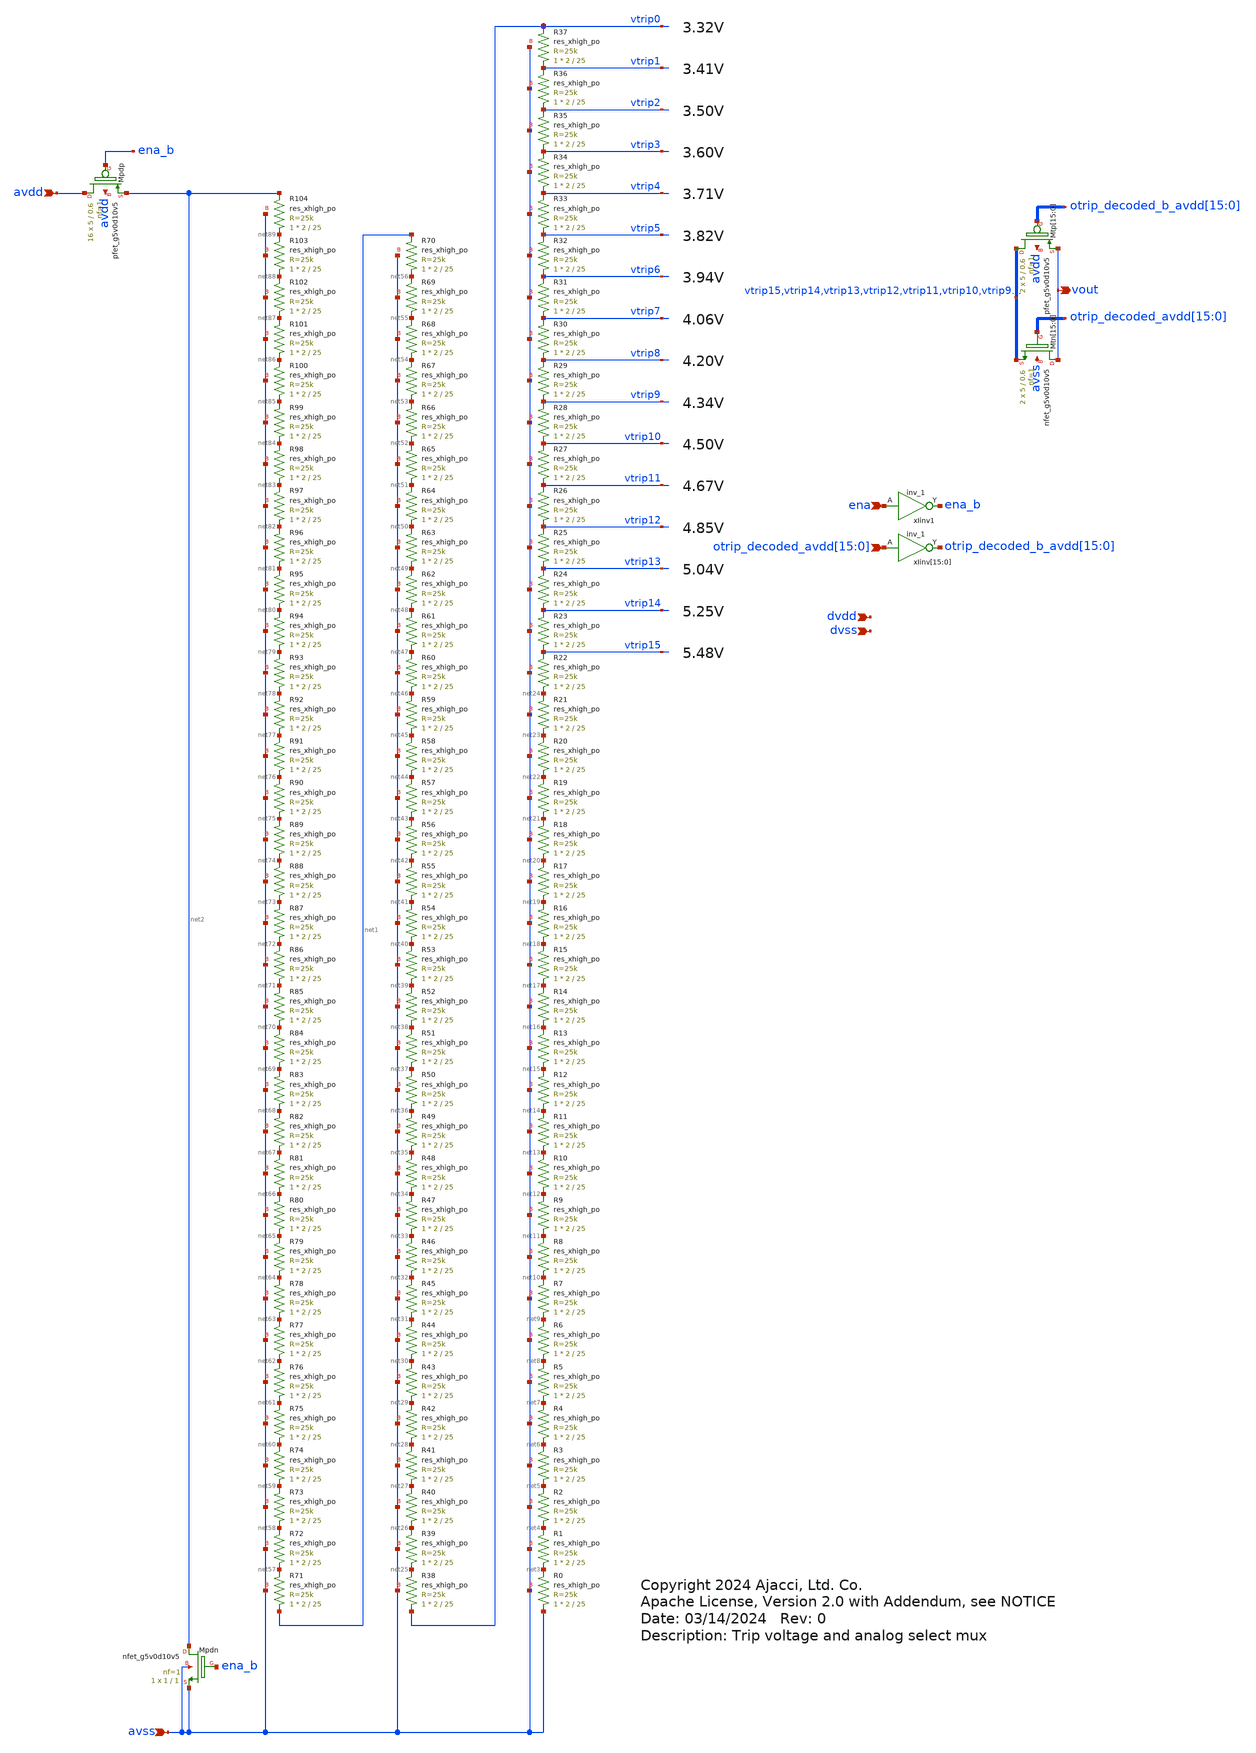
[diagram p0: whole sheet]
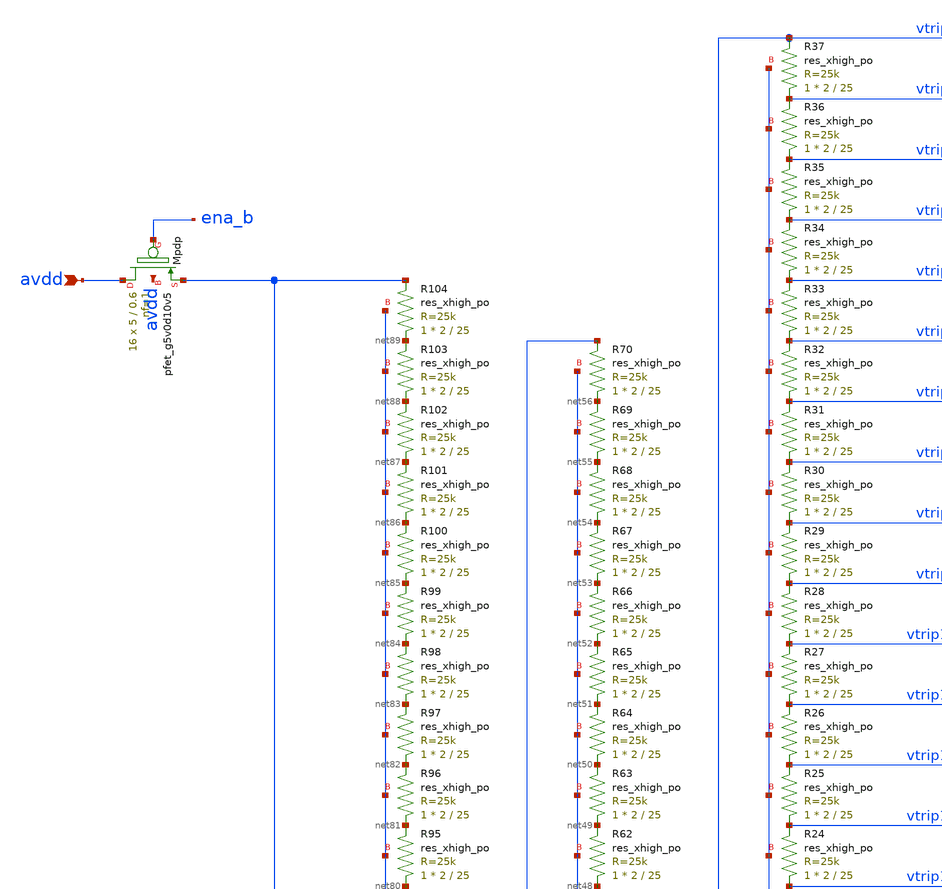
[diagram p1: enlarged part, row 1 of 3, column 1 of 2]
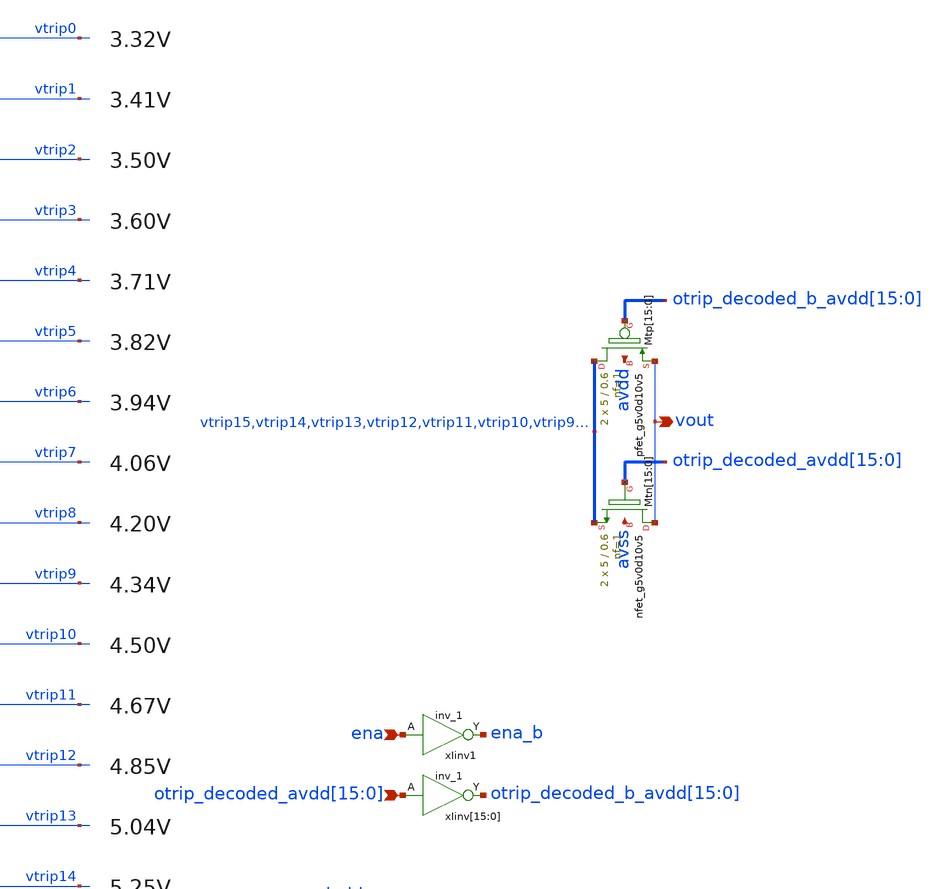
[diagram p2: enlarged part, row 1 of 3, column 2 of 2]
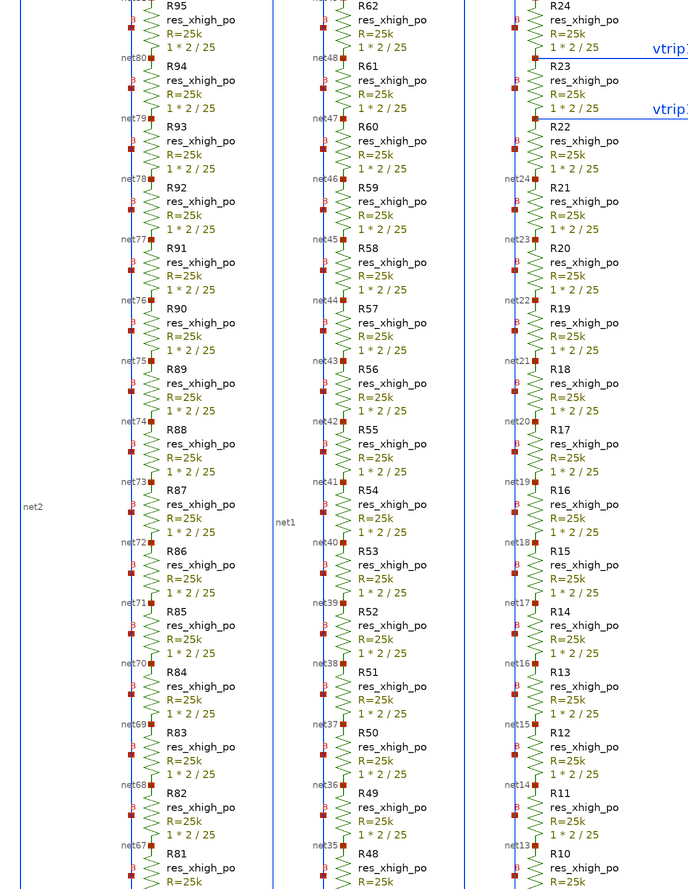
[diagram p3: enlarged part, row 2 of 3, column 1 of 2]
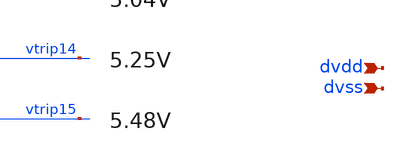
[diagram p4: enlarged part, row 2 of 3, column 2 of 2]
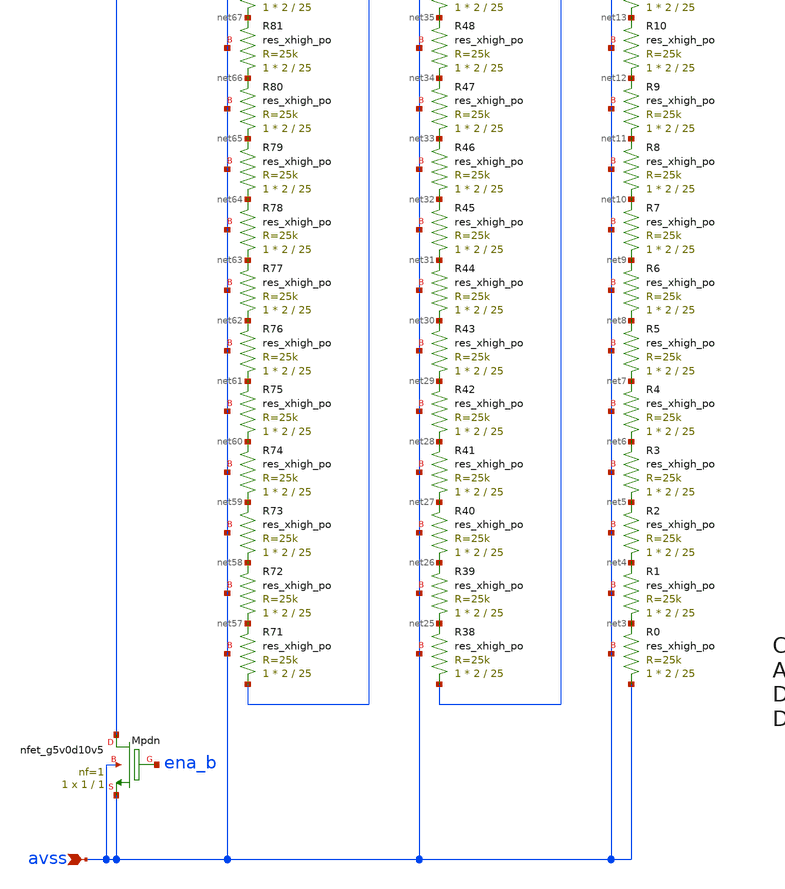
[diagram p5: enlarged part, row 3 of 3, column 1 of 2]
** sch_path: xschem/rstring_mux.sch
* Copyright 2024 Ajacci, Ltd. Co.
* Apache License, Version 2.0 with Addendum, see NOTICE
**.subckt rstring_mux vout
*+ otrip_decoded_avdd[15],otrip_decoded_avdd[14],otrip_decoded_avdd[13],otrip_decoded_avdd[12],otrip_decoded_avdd[11],otrip_decoded_avdd[10],otrip_decoded_avdd[9],otrip_decoded_avdd[8],otrip_decoded_avdd[7],otrip_decoded_avdd[6],otrip_decoded_avdd[5],otrip_decoded_avdd[4],otrip_decoded_avdd[3],otrip_decoded_avdd[2],otrip_decoded_avdd[1],otrip_decoded_avdd[0] dvss dvdd avdd avss ena
*.opin vout
*.ipin
*+ otrip_decoded_avdd[15],otrip_decoded_avdd[14],otrip_decoded_avdd[13],otrip_decoded_avdd[12],otrip_decoded_avdd[11],otrip_decoded_avdd[10],otrip_decoded_avdd[9],otrip_decoded_avdd[8],otrip_decoded_avdd[7],otrip_decoded_avdd[6],otrip_decoded_avdd[5],otrip_decoded_avdd[4],otrip_decoded_avdd[3],otrip_decoded_avdd[2],otrip_decoded_avdd[1],otrip_decoded_avdd[0]
*.ipin dvss
*.ipin dvdd
*.ipin avdd
*.ipin avss
*.ipin ena
XR1 net3 net4 avss sky130_fd_pr__res_xhigh_po W=2 L=25 mult=1 m=1
XR2 net4 net5 avss sky130_fd_pr__res_xhigh_po W=2 L=25 mult=1 m=1
XR3 net5 net6 avss sky130_fd_pr__res_xhigh_po W=2 L=25 mult=1 m=1
XR4 net6 net7 avss sky130_fd_pr__res_xhigh_po W=2 L=25 mult=1 m=1
XR5 net7 net8 avss sky130_fd_pr__res_xhigh_po W=2 L=25 mult=1 m=1
XR6 net8 net9 avss sky130_fd_pr__res_xhigh_po W=2 L=25 mult=1 m=1
XR7 net9 net10 avss sky130_fd_pr__res_xhigh_po W=2 L=25 mult=1 m=1
XR8 net10 net11 avss sky130_fd_pr__res_xhigh_po W=2 L=25 mult=1 m=1
XR9 net11 net12 avss sky130_fd_pr__res_xhigh_po W=2 L=25 mult=1 m=1
XR10 net12 net13 avss sky130_fd_pr__res_xhigh_po W=2 L=25 mult=1 m=1
XR11 net13 net14 avss sky130_fd_pr__res_xhigh_po W=2 L=25 mult=1 m=1
XR12 net14 net15 avss sky130_fd_pr__res_xhigh_po W=2 L=25 mult=1 m=1
XR13 net15 net16 avss sky130_fd_pr__res_xhigh_po W=2 L=25 mult=1 m=1
XR14 net16 net17 avss sky130_fd_pr__res_xhigh_po W=2 L=25 mult=1 m=1
XR15 net17 net18 avss sky130_fd_pr__res_xhigh_po W=2 L=25 mult=1 m=1
XR16 net18 net19 avss sky130_fd_pr__res_xhigh_po W=2 L=25 mult=1 m=1
XR17 net19 net20 avss sky130_fd_pr__res_xhigh_po W=2 L=25 mult=1 m=1
XR18 net20 net21 avss sky130_fd_pr__res_xhigh_po W=2 L=25 mult=1 m=1
XR19 net21 net22 avss sky130_fd_pr__res_xhigh_po W=2 L=25 mult=1 m=1
XR20 net22 net23 avss sky130_fd_pr__res_xhigh_po W=2 L=25 mult=1 m=1
XR21 net23 net24 avss sky130_fd_pr__res_xhigh_po W=2 L=25 mult=1 m=1
XR22 net24 vtrip15 avss sky130_fd_pr__res_xhigh_po W=2 L=25 mult=1 m=1
XR23 vtrip15 vtrip14 avss sky130_fd_pr__res_xhigh_po W=2 L=25 mult=1 m=1
XR24 vtrip14 vtrip13 avss sky130_fd_pr__res_xhigh_po W=2 L=25 mult=1 m=1
XR25 vtrip13 vtrip12 avss sky130_fd_pr__res_xhigh_po W=2 L=25 mult=1 m=1
XR26 vtrip12 vtrip11 avss sky130_fd_pr__res_xhigh_po W=2 L=25 mult=1 m=1
XR27 vtrip11 vtrip10 avss sky130_fd_pr__res_xhigh_po W=2 L=25 mult=1 m=1
XR28 vtrip10 vtrip9 avss sky130_fd_pr__res_xhigh_po W=2 L=25 mult=1 m=1
XR29 vtrip9 vtrip8 avss sky130_fd_pr__res_xhigh_po W=2 L=25 mult=1 m=1
XR30 vtrip8 vtrip7 avss sky130_fd_pr__res_xhigh_po W=2 L=25 mult=1 m=1
XR31 vtrip7 vtrip6 avss sky130_fd_pr__res_xhigh_po W=2 L=25 mult=1 m=1
XR32 vtrip6 vtrip5 avss sky130_fd_pr__res_xhigh_po W=2 L=25 mult=1 m=1
XR33 vtrip5 vtrip4 avss sky130_fd_pr__res_xhigh_po W=2 L=25 mult=1 m=1
XR34 vtrip4 vtrip3 avss sky130_fd_pr__res_xhigh_po W=2 L=25 mult=1 m=1
XR35 vtrip3 vtrip2 avss sky130_fd_pr__res_xhigh_po W=2 L=25 mult=1 m=1
XR36 vtrip2 vtrip1 avss sky130_fd_pr__res_xhigh_po W=2 L=25 mult=1 m=1
XR37 vtrip1 vtrip0 avss sky130_fd_pr__res_xhigh_po W=2 L=25 mult=1 m=1
XR38 vtrip0 net25 avss sky130_fd_pr__res_xhigh_po W=2 L=25 mult=1 m=1
XR39 net25 net26 avss sky130_fd_pr__res_xhigh_po W=2 L=25 mult=1 m=1
XR40 net26 net27 avss sky130_fd_pr__res_xhigh_po W=2 L=25 mult=1 m=1
XR41 net27 net28 avss sky130_fd_pr__res_xhigh_po W=2 L=25 mult=1 m=1
XR42 net28 net29 avss sky130_fd_pr__res_xhigh_po W=2 L=25 mult=1 m=1
XR43 net29 net30 avss sky130_fd_pr__res_xhigh_po W=2 L=25 mult=1 m=1
XR44 net30 net31 avss sky130_fd_pr__res_xhigh_po W=2 L=25 mult=1 m=1
XR45 net31 net32 avss sky130_fd_pr__res_xhigh_po W=2 L=25 mult=1 m=1
XR46 net32 net33 avss sky130_fd_pr__res_xhigh_po W=2 L=25 mult=1 m=1
XR47 net33 net34 avss sky130_fd_pr__res_xhigh_po W=2 L=25 mult=1 m=1
XR48 net34 net35 avss sky130_fd_pr__res_xhigh_po W=2 L=25 mult=1 m=1
XR49 net35 net36 avss sky130_fd_pr__res_xhigh_po W=2 L=25 mult=1 m=1
XR50 net36 net37 avss sky130_fd_pr__res_xhigh_po W=2 L=25 mult=1 m=1
XR51 net37 net38 avss sky130_fd_pr__res_xhigh_po W=2 L=25 mult=1 m=1
XR52 net38 net39 avss sky130_fd_pr__res_xhigh_po W=2 L=25 mult=1 m=1
XR53 net39 net40 avss sky130_fd_pr__res_xhigh_po W=2 L=25 mult=1 m=1
XR54 net40 net41 avss sky130_fd_pr__res_xhigh_po W=2 L=25 mult=1 m=1
XR55 net41 net42 avss sky130_fd_pr__res_xhigh_po W=2 L=25 mult=1 m=1
XR56 net42 net43 avss sky130_fd_pr__res_xhigh_po W=2 L=25 mult=1 m=1
XR57 net43 net44 avss sky130_fd_pr__res_xhigh_po W=2 L=25 mult=1 m=1
XR58 net44 net45 avss sky130_fd_pr__res_xhigh_po W=2 L=25 mult=1 m=1
XR59 net45 net46 avss sky130_fd_pr__res_xhigh_po W=2 L=25 mult=1 m=1
XR60 net46 net47 avss sky130_fd_pr__res_xhigh_po W=2 L=25 mult=1 m=1
XR61 net47 net48 avss sky130_fd_pr__res_xhigh_po W=2 L=25 mult=1 m=1
XR62 net48 net49 avss sky130_fd_pr__res_xhigh_po W=2 L=25 mult=1 m=1
XR63 net49 net50 avss sky130_fd_pr__res_xhigh_po W=2 L=25 mult=1 m=1
XR64 net50 net51 avss sky130_fd_pr__res_xhigh_po W=2 L=25 mult=1 m=1
XR65 net51 net52 avss sky130_fd_pr__res_xhigh_po W=2 L=25 mult=1 m=1
XR66 net52 net53 avss sky130_fd_pr__res_xhigh_po W=2 L=25 mult=1 m=1
XR67 net53 net54 avss sky130_fd_pr__res_xhigh_po W=2 L=25 mult=1 m=1
XR68 net54 net55 avss sky130_fd_pr__res_xhigh_po W=2 L=25 mult=1 m=1
XR69 net55 net56 avss sky130_fd_pr__res_xhigh_po W=2 L=25 mult=1 m=1
XMtp[15] vtrip15 otrip_decoded_b_avdd[15] vout avdd sky130_fd_pr__pfet_g5v0d10v5 L=0.6 W=5 nf=1 ad='int((nf+1)/2) * W/nf * 0.29'
+ as='int((nf+2)/2) * W/nf * 0.29' pd='2*int((nf+1)/2) * (W/nf + 0.29)' ps='2*int((nf+2)/2) * (W/nf + 0.29)'
+ nrd='0.29 / W' nrs='0.29 / W' sa=0 sb=0 sd=0 mult=2 m=2
XMtp[14] vtrip14 otrip_decoded_b_avdd[14] vout avdd sky130_fd_pr__pfet_g5v0d10v5 L=0.6 W=5 nf=1 ad='int((nf+1)/2) * W/nf * 0.29'
+ as='int((nf+2)/2) * W/nf * 0.29' pd='2*int((nf+1)/2) * (W/nf + 0.29)' ps='2*int((nf+2)/2) * (W/nf + 0.29)'
+ nrd='0.29 / W' nrs='0.29 / W' sa=0 sb=0 sd=0 mult=2 m=2
XMtp[13] vtrip13 otrip_decoded_b_avdd[13] vout avdd sky130_fd_pr__pfet_g5v0d10v5 L=0.6 W=5 nf=1 ad='int((nf+1)/2) * W/nf * 0.29'
+ as='int((nf+2)/2) * W/nf * 0.29' pd='2*int((nf+1)/2) * (W/nf + 0.29)' ps='2*int((nf+2)/2) * (W/nf + 0.29)'
+ nrd='0.29 / W' nrs='0.29 / W' sa=0 sb=0 sd=0 mult=2 m=2
XMtp[12] vtrip12 otrip_decoded_b_avdd[12] vout avdd sky130_fd_pr__pfet_g5v0d10v5 L=0.6 W=5 nf=1 ad='int((nf+1)/2) * W/nf * 0.29'
+ as='int((nf+2)/2) * W/nf * 0.29' pd='2*int((nf+1)/2) * (W/nf + 0.29)' ps='2*int((nf+2)/2) * (W/nf + 0.29)'
+ nrd='0.29 / W' nrs='0.29 / W' sa=0 sb=0 sd=0 mult=2 m=2
XMtp[11] vtrip11 otrip_decoded_b_avdd[11] vout avdd sky130_fd_pr__pfet_g5v0d10v5 L=0.6 W=5 nf=1 ad='int((nf+1)/2) * W/nf * 0.29'
+ as='int((nf+2)/2) * W/nf * 0.29' pd='2*int((nf+1)/2) * (W/nf + 0.29)' ps='2*int((nf+2)/2) * (W/nf + 0.29)'
+ nrd='0.29 / W' nrs='0.29 / W' sa=0 sb=0 sd=0 mult=2 m=2
XMtp[10] vtrip10 otrip_decoded_b_avdd[10] vout avdd sky130_fd_pr__pfet_g5v0d10v5 L=0.6 W=5 nf=1 ad='int((nf+1)/2) * W/nf * 0.29'
+ as='int((nf+2)/2) * W/nf * 0.29' pd='2*int((nf+1)/2) * (W/nf + 0.29)' ps='2*int((nf+2)/2) * (W/nf + 0.29)'
+ nrd='0.29 / W' nrs='0.29 / W' sa=0 sb=0 sd=0 mult=2 m=2
XMtp[9] vtrip9 otrip_decoded_b_avdd[9] vout avdd sky130_fd_pr__pfet_g5v0d10v5 L=0.6 W=5 nf=1 ad='int((nf+1)/2) * W/nf * 0.29'
+ as='int((nf+2)/2) * W/nf * 0.29' pd='2*int((nf+1)/2) * (W/nf + 0.29)' ps='2*int((nf+2)/2) * (W/nf + 0.29)'
+ nrd='0.29 / W' nrs='0.29 / W' sa=0 sb=0 sd=0 mult=2 m=2
XMtp[8] vtrip8 otrip_decoded_b_avdd[8] vout avdd sky130_fd_pr__pfet_g5v0d10v5 L=0.6 W=5 nf=1 ad='int((nf+1)/2) * W/nf * 0.29'
+ as='int((nf+2)/2) * W/nf * 0.29' pd='2*int((nf+1)/2) * (W/nf + 0.29)' ps='2*int((nf+2)/2) * (W/nf + 0.29)'
+ nrd='0.29 / W' nrs='0.29 / W' sa=0 sb=0 sd=0 mult=2 m=2
XMtp[7] vtrip7 otrip_decoded_b_avdd[7] vout avdd sky130_fd_pr__pfet_g5v0d10v5 L=0.6 W=5 nf=1 ad='int((nf+1)/2) * W/nf * 0.29'
+ as='int((nf+2)/2) * W/nf * 0.29' pd='2*int((nf+1)/2) * (W/nf + 0.29)' ps='2*int((nf+2)/2) * (W/nf + 0.29)'
+ nrd='0.29 / W' nrs='0.29 / W' sa=0 sb=0 sd=0 mult=2 m=2
XMtp[6] vtrip6 otrip_decoded_b_avdd[6] vout avdd sky130_fd_pr__pfet_g5v0d10v5 L=0.6 W=5 nf=1 ad='int((nf+1)/2) * W/nf * 0.29'
+ as='int((nf+2)/2) * W/nf * 0.29' pd='2*int((nf+1)/2) * (W/nf + 0.29)' ps='2*int((nf+2)/2) * (W/nf + 0.29)'
+ nrd='0.29 / W' nrs='0.29 / W' sa=0 sb=0 sd=0 mult=2 m=2
XMtp[5] vtrip5 otrip_decoded_b_avdd[5] vout avdd sky130_fd_pr__pfet_g5v0d10v5 L=0.6 W=5 nf=1 ad='int((nf+1)/2) * W/nf * 0.29'
+ as='int((nf+2)/2) * W/nf * 0.29' pd='2*int((nf+1)/2) * (W/nf + 0.29)' ps='2*int((nf+2)/2) * (W/nf + 0.29)'
+ nrd='0.29 / W' nrs='0.29 / W' sa=0 sb=0 sd=0 mult=2 m=2
XMtp[4] vtrip4 otrip_decoded_b_avdd[4] vout avdd sky130_fd_pr__pfet_g5v0d10v5 L=0.6 W=5 nf=1 ad='int((nf+1)/2) * W/nf * 0.29'
+ as='int((nf+2)/2) * W/nf * 0.29' pd='2*int((nf+1)/2) * (W/nf + 0.29)' ps='2*int((nf+2)/2) * (W/nf + 0.29)'
+ nrd='0.29 / W' nrs='0.29 / W' sa=0 sb=0 sd=0 mult=2 m=2
XMtp[3] vtrip3 otrip_decoded_b_avdd[3] vout avdd sky130_fd_pr__pfet_g5v0d10v5 L=0.6 W=5 nf=1 ad='int((nf+1)/2) * W/nf * 0.29'
+ as='int((nf+2)/2) * W/nf * 0.29' pd='2*int((nf+1)/2) * (W/nf + 0.29)' ps='2*int((nf+2)/2) * (W/nf + 0.29)'
+ nrd='0.29 / W' nrs='0.29 / W' sa=0 sb=0 sd=0 mult=2 m=2
XMtp[2] vtrip2 otrip_decoded_b_avdd[2] vout avdd sky130_fd_pr__pfet_g5v0d10v5 L=0.6 W=5 nf=1 ad='int((nf+1)/2) * W/nf * 0.29'
+ as='int((nf+2)/2) * W/nf * 0.29' pd='2*int((nf+1)/2) * (W/nf + 0.29)' ps='2*int((nf+2)/2) * (W/nf + 0.29)'
+ nrd='0.29 / W' nrs='0.29 / W' sa=0 sb=0 sd=0 mult=2 m=2
XMtp[1] vtrip1 otrip_decoded_b_avdd[1] vout avdd sky130_fd_pr__pfet_g5v0d10v5 L=0.6 W=5 nf=1 ad='int((nf+1)/2) * W/nf * 0.29'
+ as='int((nf+2)/2) * W/nf * 0.29' pd='2*int((nf+1)/2) * (W/nf + 0.29)' ps='2*int((nf+2)/2) * (W/nf + 0.29)'
+ nrd='0.29 / W' nrs='0.29 / W' sa=0 sb=0 sd=0 mult=2 m=2
XMtp[0] vtrip0 otrip_decoded_b_avdd[0] vout avdd sky130_fd_pr__pfet_g5v0d10v5 L=0.6 W=5 nf=1 ad='int((nf+1)/2) * W/nf * 0.29'
+ as='int((nf+2)/2) * W/nf * 0.29' pd='2*int((nf+1)/2) * (W/nf + 0.29)' ps='2*int((nf+2)/2) * (W/nf + 0.29)'
+ nrd='0.29 / W' nrs='0.29 / W' sa=0 sb=0 sd=0 mult=2 m=2
XMtn[15] vout otrip_decoded_avdd[15] vtrip15 avss sky130_fd_pr__nfet_g5v0d10v5 L=0.6 W=5 nf=1 ad='int((nf+1)/2) * W/nf * 0.29'
+ as='int((nf+2)/2) * W/nf * 0.29' pd='2*int((nf+1)/2) * (W/nf + 0.29)' ps='2*int((nf+2)/2) * (W/nf + 0.29)'
+ nrd='0.29 / W' nrs='0.29 / W' sa=0 sb=0 sd=0 mult=2 m=2
XMtn[14] vout otrip_decoded_avdd[14] vtrip14 avss sky130_fd_pr__nfet_g5v0d10v5 L=0.6 W=5 nf=1 ad='int((nf+1)/2) * W/nf * 0.29'
+ as='int((nf+2)/2) * W/nf * 0.29' pd='2*int((nf+1)/2) * (W/nf + 0.29)' ps='2*int((nf+2)/2) * (W/nf + 0.29)'
+ nrd='0.29 / W' nrs='0.29 / W' sa=0 sb=0 sd=0 mult=2 m=2
XMtn[13] vout otrip_decoded_avdd[13] vtrip13 avss sky130_fd_pr__nfet_g5v0d10v5 L=0.6 W=5 nf=1 ad='int((nf+1)/2) * W/nf * 0.29'
+ as='int((nf+2)/2) * W/nf * 0.29' pd='2*int((nf+1)/2) * (W/nf + 0.29)' ps='2*int((nf+2)/2) * (W/nf + 0.29)'
+ nrd='0.29 / W' nrs='0.29 / W' sa=0 sb=0 sd=0 mult=2 m=2
XMtn[12] vout otrip_decoded_avdd[12] vtrip12 avss sky130_fd_pr__nfet_g5v0d10v5 L=0.6 W=5 nf=1 ad='int((nf+1)/2) * W/nf * 0.29'
+ as='int((nf+2)/2) * W/nf * 0.29' pd='2*int((nf+1)/2) * (W/nf + 0.29)' ps='2*int((nf+2)/2) * (W/nf + 0.29)'
+ nrd='0.29 / W' nrs='0.29 / W' sa=0 sb=0 sd=0 mult=2 m=2
XMtn[11] vout otrip_decoded_avdd[11] vtrip11 avss sky130_fd_pr__nfet_g5v0d10v5 L=0.6 W=5 nf=1 ad='int((nf+1)/2) * W/nf * 0.29'
+ as='int((nf+2)/2) * W/nf * 0.29' pd='2*int((nf+1)/2) * (W/nf + 0.29)' ps='2*int((nf+2)/2) * (W/nf + 0.29)'
+ nrd='0.29 / W' nrs='0.29 / W' sa=0 sb=0 sd=0 mult=2 m=2
XMtn[10] vout otrip_decoded_avdd[10] vtrip10 avss sky130_fd_pr__nfet_g5v0d10v5 L=0.6 W=5 nf=1 ad='int((nf+1)/2) * W/nf * 0.29'
+ as='int((nf+2)/2) * W/nf * 0.29' pd='2*int((nf+1)/2) * (W/nf + 0.29)' ps='2*int((nf+2)/2) * (W/nf + 0.29)'
+ nrd='0.29 / W' nrs='0.29 / W' sa=0 sb=0 sd=0 mult=2 m=2
XMtn[9] vout otrip_decoded_avdd[9] vtrip9 avss sky130_fd_pr__nfet_g5v0d10v5 L=0.6 W=5 nf=1 ad='int((nf+1)/2) * W/nf * 0.29'
+ as='int((nf+2)/2) * W/nf * 0.29' pd='2*int((nf+1)/2) * (W/nf + 0.29)' ps='2*int((nf+2)/2) * (W/nf + 0.29)'
+ nrd='0.29 / W' nrs='0.29 / W' sa=0 sb=0 sd=0 mult=2 m=2
XMtn[8] vout otrip_decoded_avdd[8] vtrip8 avss sky130_fd_pr__nfet_g5v0d10v5 L=0.6 W=5 nf=1 ad='int((nf+1)/2) * W/nf * 0.29'
+ as='int((nf+2)/2) * W/nf * 0.29' pd='2*int((nf+1)/2) * (W/nf + 0.29)' ps='2*int((nf+2)/2) * (W/nf + 0.29)'
+ nrd='0.29 / W' nrs='0.29 / W' sa=0 sb=0 sd=0 mult=2 m=2
XMtn[7] vout otrip_decoded_avdd[7] vtrip7 avss sky130_fd_pr__nfet_g5v0d10v5 L=0.6 W=5 nf=1 ad='int((nf+1)/2) * W/nf * 0.29'
+ as='int((nf+2)/2) * W/nf * 0.29' pd='2*int((nf+1)/2) * (W/nf + 0.29)' ps='2*int((nf+2)/2) * (W/nf + 0.29)'
+ nrd='0.29 / W' nrs='0.29 / W' sa=0 sb=0 sd=0 mult=2 m=2
XMtn[6] vout otrip_decoded_avdd[6] vtrip6 avss sky130_fd_pr__nfet_g5v0d10v5 L=0.6 W=5 nf=1 ad='int((nf+1)/2) * W/nf * 0.29'
+ as='int((nf+2)/2) * W/nf * 0.29' pd='2*int((nf+1)/2) * (W/nf + 0.29)' ps='2*int((nf+2)/2) * (W/nf + 0.29)'
+ nrd='0.29 / W' nrs='0.29 / W' sa=0 sb=0 sd=0 mult=2 m=2
XMtn[5] vout otrip_decoded_avdd[5] vtrip5 avss sky130_fd_pr__nfet_g5v0d10v5 L=0.6 W=5 nf=1 ad='int((nf+1)/2) * W/nf * 0.29'
+ as='int((nf+2)/2) * W/nf * 0.29' pd='2*int((nf+1)/2) * (W/nf + 0.29)' ps='2*int((nf+2)/2) * (W/nf + 0.29)'
+ nrd='0.29 / W' nrs='0.29 / W' sa=0 sb=0 sd=0 mult=2 m=2
XMtn[4] vout otrip_decoded_avdd[4] vtrip4 avss sky130_fd_pr__nfet_g5v0d10v5 L=0.6 W=5 nf=1 ad='int((nf+1)/2) * W/nf * 0.29'
+ as='int((nf+2)/2) * W/nf * 0.29' pd='2*int((nf+1)/2) * (W/nf + 0.29)' ps='2*int((nf+2)/2) * (W/nf + 0.29)'
+ nrd='0.29 / W' nrs='0.29 / W' sa=0 sb=0 sd=0 mult=2 m=2
XMtn[3] vout otrip_decoded_avdd[3] vtrip3 avss sky130_fd_pr__nfet_g5v0d10v5 L=0.6 W=5 nf=1 ad='int((nf+1)/2) * W/nf * 0.29'
+ as='int((nf+2)/2) * W/nf * 0.29' pd='2*int((nf+1)/2) * (W/nf + 0.29)' ps='2*int((nf+2)/2) * (W/nf + 0.29)'
+ nrd='0.29 / W' nrs='0.29 / W' sa=0 sb=0 sd=0 mult=2 m=2
XMtn[2] vout otrip_decoded_avdd[2] vtrip2 avss sky130_fd_pr__nfet_g5v0d10v5 L=0.6 W=5 nf=1 ad='int((nf+1)/2) * W/nf * 0.29'
+ as='int((nf+2)/2) * W/nf * 0.29' pd='2*int((nf+1)/2) * (W/nf + 0.29)' ps='2*int((nf+2)/2) * (W/nf + 0.29)'
+ nrd='0.29 / W' nrs='0.29 / W' sa=0 sb=0 sd=0 mult=2 m=2
XMtn[1] vout otrip_decoded_avdd[1] vtrip1 avss sky130_fd_pr__nfet_g5v0d10v5 L=0.6 W=5 nf=1 ad='int((nf+1)/2) * W/nf * 0.29'
+ as='int((nf+2)/2) * W/nf * 0.29' pd='2*int((nf+1)/2) * (W/nf + 0.29)' ps='2*int((nf+2)/2) * (W/nf + 0.29)'
+ nrd='0.29 / W' nrs='0.29 / W' sa=0 sb=0 sd=0 mult=2 m=2
XMtn[0] vout otrip_decoded_avdd[0] vtrip0 avss sky130_fd_pr__nfet_g5v0d10v5 L=0.6 W=5 nf=1 ad='int((nf+1)/2) * W/nf * 0.29'
+ as='int((nf+2)/2) * W/nf * 0.29' pd='2*int((nf+1)/2) * (W/nf + 0.29)' ps='2*int((nf+2)/2) * (W/nf + 0.29)'
+ nrd='0.29 / W' nrs='0.29 / W' sa=0 sb=0 sd=0 mult=2 m=2
XR70 net56 net1 avss sky130_fd_pr__res_xhigh_po W=2 L=25 mult=1 m=1
XR71 net1 net57 avss sky130_fd_pr__res_xhigh_po W=2 L=25 mult=1 m=1
XR72 net57 net58 avss sky130_fd_pr__res_xhigh_po W=2 L=25 mult=1 m=1
XR73 net58 net59 avss sky130_fd_pr__res_xhigh_po W=2 L=25 mult=1 m=1
XR74 net59 net60 avss sky130_fd_pr__res_xhigh_po W=2 L=25 mult=1 m=1
XR75 net60 net61 avss sky130_fd_pr__res_xhigh_po W=2 L=25 mult=1 m=1
XR76 net61 net62 avss sky130_fd_pr__res_xhigh_po W=2 L=25 mult=1 m=1
XR77 net62 net63 avss sky130_fd_pr__res_xhigh_po W=2 L=25 mult=1 m=1
XR78 net63 net64 avss sky130_fd_pr__res_xhigh_po W=2 L=25 mult=1 m=1
XR79 net64 net65 avss sky130_fd_pr__res_xhigh_po W=2 L=25 mult=1 m=1
XR80 net65 net66 avss sky130_fd_pr__res_xhigh_po W=2 L=25 mult=1 m=1
XR81 net66 net67 avss sky130_fd_pr__res_xhigh_po W=2 L=25 mult=1 m=1
XR82 net67 net68 avss sky130_fd_pr__res_xhigh_po W=2 L=25 mult=1 m=1
XR83 net68 net69 avss sky130_fd_pr__res_xhigh_po W=2 L=25 mult=1 m=1
XR84 net69 net70 avss sky130_fd_pr__res_xhigh_po W=2 L=25 mult=1 m=1
XR85 net70 net71 avss sky130_fd_pr__res_xhigh_po W=2 L=25 mult=1 m=1
XR86 net71 net72 avss sky130_fd_pr__res_xhigh_po W=2 L=25 mult=1 m=1
XR87 net72 net73 avss sky130_fd_pr__res_xhigh_po W=2 L=25 mult=1 m=1
XR88 net73 net74 avss sky130_fd_pr__res_xhigh_po W=2 L=25 mult=1 m=1
XR89 net74 net75 avss sky130_fd_pr__res_xhigh_po W=2 L=25 mult=1 m=1
XR90 net75 net76 avss sky130_fd_pr__res_xhigh_po W=2 L=25 mult=1 m=1
XR91 net76 net77 avss sky130_fd_pr__res_xhigh_po W=2 L=25 mult=1 m=1
XR92 net77 net78 avss sky130_fd_pr__res_xhigh_po W=2 L=25 mult=1 m=1
XR93 net78 net79 avss sky130_fd_pr__res_xhigh_po W=2 L=25 mult=1 m=1
XR94 net79 net80 avss sky130_fd_pr__res_xhigh_po W=2 L=25 mult=1 m=1
XR95 net80 net81 avss sky130_fd_pr__res_xhigh_po W=2 L=25 mult=1 m=1
XR96 net81 net82 avss sky130_fd_pr__res_xhigh_po W=2 L=25 mult=1 m=1
XR97 net82 net83 avss sky130_fd_pr__res_xhigh_po W=2 L=25 mult=1 m=1
XR98 net83 net84 avss sky130_fd_pr__res_xhigh_po W=2 L=25 mult=1 m=1
XR99 net84 net85 avss sky130_fd_pr__res_xhigh_po W=2 L=25 mult=1 m=1
XR100 net85 net86 avss sky130_fd_pr__res_xhigh_po W=2 L=25 mult=1 m=1
XR101 net86 net87 avss sky130_fd_pr__res_xhigh_po W=2 L=25 mult=1 m=1
XR102 net87 net88 avss sky130_fd_pr__res_xhigh_po W=2 L=25 mult=1 m=1
XR103 net88 net89 avss sky130_fd_pr__res_xhigh_po W=2 L=25 mult=1 m=1
xIinv[15] otrip_decoded_avdd[15] avss avss avdd avdd otrip_decoded_b_avdd[15]
+ sky130_fd_sc_hvl__inv_1
xIinv[14] otrip_decoded_avdd[14] avss avss avdd avdd otrip_decoded_b_avdd[14]
+ sky130_fd_sc_hvl__inv_1
xIinv[13] otrip_decoded_avdd[13] avss avss avdd avdd otrip_decoded_b_avdd[13]
+ sky130_fd_sc_hvl__inv_1
xIinv[12] otrip_decoded_avdd[12] avss avss avdd avdd otrip_decoded_b_avdd[12]
+ sky130_fd_sc_hvl__inv_1
xIinv[11] otrip_decoded_avdd[11] avss avss avdd avdd otrip_decoded_b_avdd[11]
+ sky130_fd_sc_hvl__inv_1
xIinv[10] otrip_decoded_avdd[10] avss avss avdd avdd otrip_decoded_b_avdd[10]
+ sky130_fd_sc_hvl__inv_1
xIinv[9] otrip_decoded_avdd[9] avss avss avdd avdd otrip_decoded_b_avdd[9] sky130_fd_sc_hvl__inv_1
xIinv[8] otrip_decoded_avdd[8] avss avss avdd avdd otrip_decoded_b_avdd[8] sky130_fd_sc_hvl__inv_1
xIinv[7] otrip_decoded_avdd[7] avss avss avdd avdd otrip_decoded_b_avdd[7] sky130_fd_sc_hvl__inv_1
xIinv[6] otrip_decoded_avdd[6] avss avss avdd avdd otrip_decoded_b_avdd[6] sky130_fd_sc_hvl__inv_1
xIinv[5] otrip_decoded_avdd[5] avss avss avdd avdd otrip_decoded_b_avdd[5] sky130_fd_sc_hvl__inv_1
xIinv[4] otrip_decoded_avdd[4] avss avss avdd avdd otrip_decoded_b_avdd[4] sky130_fd_sc_hvl__inv_1
xIinv[3] otrip_decoded_avdd[3] avss avss avdd avdd otrip_decoded_b_avdd[3] sky130_fd_sc_hvl__inv_1
xIinv[2] otrip_decoded_avdd[2] avss avss avdd avdd otrip_decoded_b_avdd[2] sky130_fd_sc_hvl__inv_1
xIinv[1] otrip_decoded_avdd[1] avss avss avdd avdd otrip_decoded_b_avdd[1] sky130_fd_sc_hvl__inv_1
xIinv[0] otrip_decoded_avdd[0] avss avss avdd avdd otrip_decoded_b_avdd[0] sky130_fd_sc_hvl__inv_1
XR0 avss net3 avss sky130_fd_pr__res_xhigh_po W=2 L=25 mult=1 m=1
XR104 net89 net2 avss sky130_fd_pr__res_xhigh_po W=2 L=25 mult=1 m=1
XMpdn net2 ena_b avss avss sky130_fd_pr__nfet_g5v0d10v5 L=1 W=1 nf=1 ad='int((nf+1)/2) * W/nf * 0.29'
+ as='int((nf+2)/2) * W/nf * 0.29' pd='2*int((nf+1)/2) * (W/nf + 0.29)' ps='2*int((nf+2)/2) * (W/nf + 0.29)'
+ nrd='0.29 / W' nrs='0.29 / W' sa=0 sb=0 sd=0 mult=1 m=1
XMpdp avdd ena_b net2 avdd sky130_fd_pr__pfet_g5v0d10v5 L=0.6 W=5 nf=1 ad='int((nf+1)/2) * W/nf * 0.29'
+ as='int((nf+2)/2) * W/nf * 0.29' pd='2*int((nf+1)/2) * (W/nf + 0.29)' ps='2*int((nf+2)/2) * (W/nf + 0.29)'
+ nrd='0.29 / W' nrs='0.29 / W' sa=0 sb=0 sd=0 mult=16 m=16
xIinv1 ena avss avss avdd avdd ena_b sky130_fd_sc_hvl__inv_1
**.ends
.end
